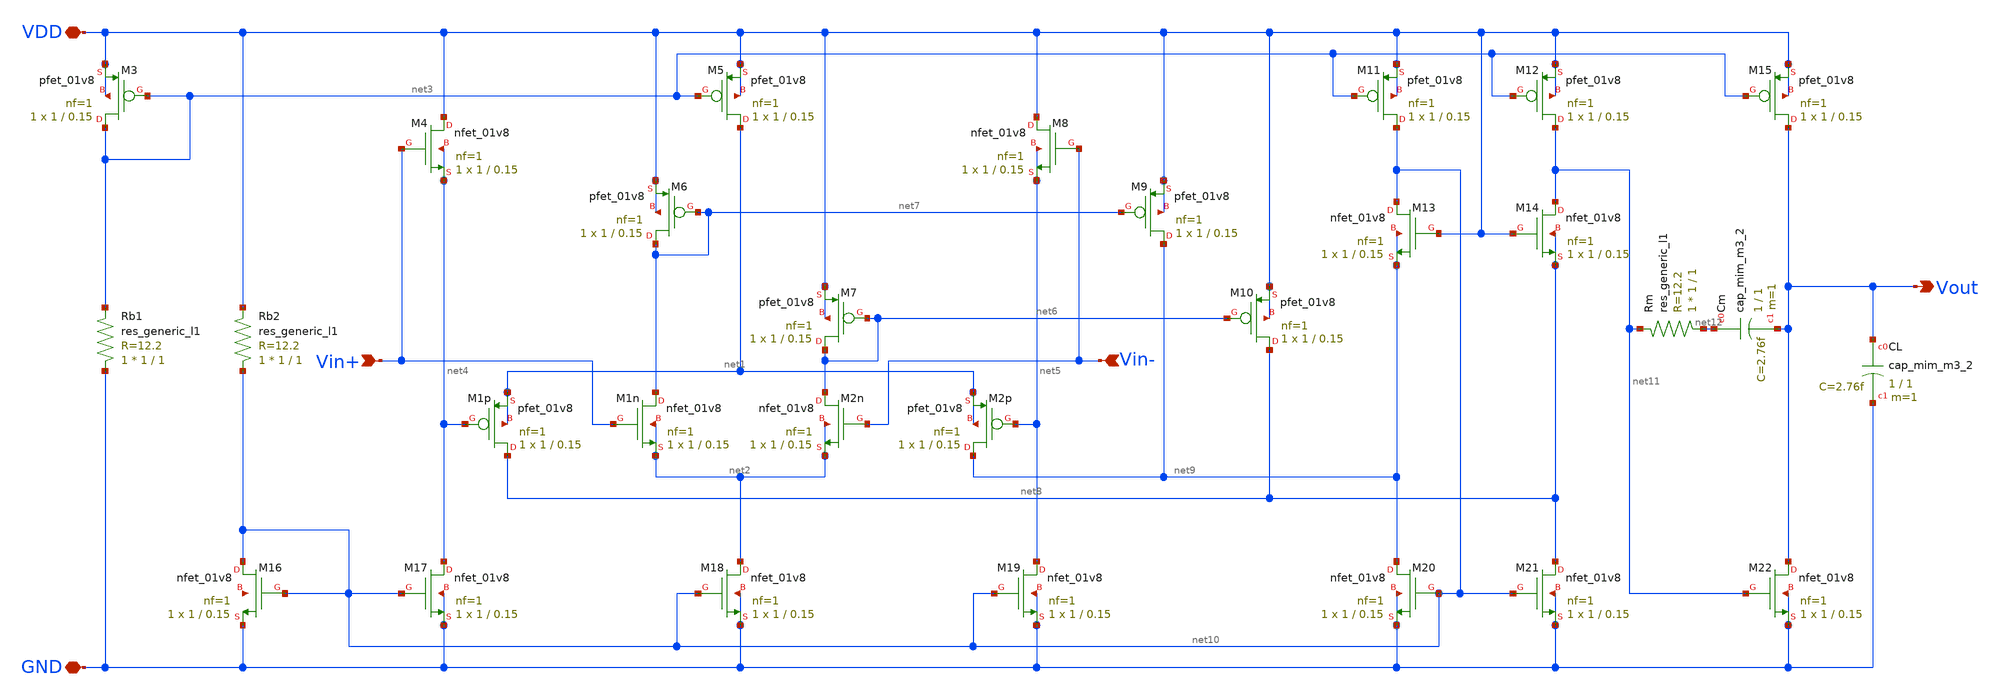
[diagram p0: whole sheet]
** sch_path: charge-pump/charge-pump-amplifier.sch
**.subckt charge-pump-amplifier Vin+ Vin- Vout VDD GND
*.ipin Vin+
*.ipin Vin-
*.opin Vout
*.iopin VDD
*.iopin GND
XM1p net8 net4 net1 net1 sky130_fd_pr__pfet_01v8 L=0.15 W=1 nf=1 ad='int((nf+1)/2) * W/nf * 0.29' as='int((nf+2)/2) * W/nf * 0.29'
+ pd='2*int((nf+1)/2) * (W/nf + 0.29)' ps='2*int((nf+2)/2) * (W/nf + 0.29)' nrd='0.29 / W' nrs='0.29 / W'
+ sa=0 sb=0 sd=0 mult=1 m=1
XM1n net7 Vin+ net2 net2 sky130_fd_pr__nfet_01v8 L=0.15 W=1 nf=1 ad='int((nf+1)/2) * W/nf * 0.29' as='int((nf+2)/2) * W/nf * 0.29'
+ pd='2*int((nf+1)/2) * (W/nf + 0.29)' ps='2*int((nf+2)/2) * (W/nf + 0.29)' nrd='0.29 / W' nrs='0.29 / W'
+ sa=0 sb=0 sd=0 mult=1 m=1
XM2n net6 Vin- net2 net2 sky130_fd_pr__nfet_01v8 L=0.15 W=1 nf=1 ad='int((nf+1)/2) * W/nf * 0.29' as='int((nf+2)/2) * W/nf * 0.29'
+ pd='2*int((nf+1)/2) * (W/nf + 0.29)' ps='2*int((nf+2)/2) * (W/nf + 0.29)' nrd='0.29 / W' nrs='0.29 / W'
+ sa=0 sb=0 sd=0 mult=1 m=1
XM2p net9 net5 net1 net1 sky130_fd_pr__pfet_01v8 L=0.15 W=1 nf=1 ad='int((nf+1)/2) * W/nf * 0.29' as='int((nf+2)/2) * W/nf * 0.29'
+ pd='2*int((nf+1)/2) * (W/nf + 0.29)' ps='2*int((nf+2)/2) * (W/nf + 0.29)' nrd='0.29 / W' nrs='0.29 / W'
+ sa=0 sb=0 sd=0 mult=1 m=1
XM3 net3 net3 VDD VDD sky130_fd_pr__pfet_01v8 L=0.15 W=1 nf=1 ad='int((nf+1)/2) * W/nf * 0.29' as='int((nf+2)/2) * W/nf * 0.29'
+ pd='2*int((nf+1)/2) * (W/nf + 0.29)' ps='2*int((nf+2)/2) * (W/nf + 0.29)' nrd='0.29 / W' nrs='0.29 / W'
+ sa=0 sb=0 sd=0 mult=1 m=1
XM4 VDD Vin+ net4 net4 sky130_fd_pr__nfet_01v8 L=0.15 W=1 nf=1 ad='int((nf+1)/2) * W/nf * 0.29' as='int((nf+2)/2) * W/nf * 0.29'
+ pd='2*int((nf+1)/2) * (W/nf + 0.29)' ps='2*int((nf+2)/2) * (W/nf + 0.29)' nrd='0.29 / W' nrs='0.29 / W'
+ sa=0 sb=0 sd=0 mult=1 m=1
XM5 net1 net3 VDD VDD sky130_fd_pr__pfet_01v8 L=0.15 W=1 nf=1 ad='int((nf+1)/2) * W/nf * 0.29' as='int((nf+2)/2) * W/nf * 0.29'
+ pd='2*int((nf+1)/2) * (W/nf + 0.29)' ps='2*int((nf+2)/2) * (W/nf + 0.29)' nrd='0.29 / W' nrs='0.29 / W'
+ sa=0 sb=0 sd=0 mult=1 m=1
XM6 net7 net7 VDD VDD sky130_fd_pr__pfet_01v8 L=0.15 W=1 nf=1 ad='int((nf+1)/2) * W/nf * 0.29' as='int((nf+2)/2) * W/nf * 0.29'
+ pd='2*int((nf+1)/2) * (W/nf + 0.29)' ps='2*int((nf+2)/2) * (W/nf + 0.29)' nrd='0.29 / W' nrs='0.29 / W'
+ sa=0 sb=0 sd=0 mult=1 m=1
XM7 net6 net6 VDD VDD sky130_fd_pr__pfet_01v8 L=0.15 W=1 nf=1 ad='int((nf+1)/2) * W/nf * 0.29' as='int((nf+2)/2) * W/nf * 0.29'
+ pd='2*int((nf+1)/2) * (W/nf + 0.29)' ps='2*int((nf+2)/2) * (W/nf + 0.29)' nrd='0.29 / W' nrs='0.29 / W'
+ sa=0 sb=0 sd=0 mult=1 m=1
XM8 VDD Vin- net5 net5 sky130_fd_pr__nfet_01v8 L=0.15 W=1 nf=1 ad='int((nf+1)/2) * W/nf * 0.29' as='int((nf+2)/2) * W/nf * 0.29'
+ pd='2*int((nf+1)/2) * (W/nf + 0.29)' ps='2*int((nf+2)/2) * (W/nf + 0.29)' nrd='0.29 / W' nrs='0.29 / W'
+ sa=0 sb=0 sd=0 mult=1 m=1
XM9 net9 net7 VDD VDD sky130_fd_pr__pfet_01v8 L=0.15 W=1 nf=1 ad='int((nf+1)/2) * W/nf * 0.29' as='int((nf+2)/2) * W/nf * 0.29'
+ pd='2*int((nf+1)/2) * (W/nf + 0.29)' ps='2*int((nf+2)/2) * (W/nf + 0.29)' nrd='0.29 / W' nrs='0.29 / W'
+ sa=0 sb=0 sd=0 mult=1 m=1
XM10 net8 net6 VDD VDD sky130_fd_pr__pfet_01v8 L=0.15 W=1 nf=1 ad='int((nf+1)/2) * W/nf * 0.29' as='int((nf+2)/2) * W/nf * 0.29'
+ pd='2*int((nf+1)/2) * (W/nf + 0.29)' ps='2*int((nf+2)/2) * (W/nf + 0.29)' nrd='0.29 / W' nrs='0.29 / W'
+ sa=0 sb=0 sd=0 mult=1 m=1
XM11 net10 net3 VDD VDD sky130_fd_pr__pfet_01v8 L=0.15 W=1 nf=1 ad='int((nf+1)/2) * W/nf * 0.29' as='int((nf+2)/2) * W/nf * 0.29'
+ pd='2*int((nf+1)/2) * (W/nf + 0.29)' ps='2*int((nf+2)/2) * (W/nf + 0.29)' nrd='0.29 / W' nrs='0.29 / W'
+ sa=0 sb=0 sd=0 mult=1 m=1
XM12 net11 net3 VDD VDD sky130_fd_pr__pfet_01v8 L=0.15 W=1 nf=1 ad='int((nf+1)/2) * W/nf * 0.29' as='int((nf+2)/2) * W/nf * 0.29'
+ pd='2*int((nf+1)/2) * (W/nf + 0.29)' ps='2*int((nf+2)/2) * (W/nf + 0.29)' nrd='0.29 / W' nrs='0.29 / W'
+ sa=0 sb=0 sd=0 mult=1 m=1
XM13 net10 VDD net9 net9 sky130_fd_pr__nfet_01v8 L=0.15 W=1 nf=1 ad='int((nf+1)/2) * W/nf * 0.29' as='int((nf+2)/2) * W/nf * 0.29'
+ pd='2*int((nf+1)/2) * (W/nf + 0.29)' ps='2*int((nf+2)/2) * (W/nf + 0.29)' nrd='0.29 / W' nrs='0.29 / W'
+ sa=0 sb=0 sd=0 mult=1 m=1
XM14 net11 VDD net8 net8 sky130_fd_pr__nfet_01v8 L=0.15 W=1 nf=1 ad='int((nf+1)/2) * W/nf * 0.29' as='int((nf+2)/2) * W/nf * 0.29'
+ pd='2*int((nf+1)/2) * (W/nf + 0.29)' ps='2*int((nf+2)/2) * (W/nf + 0.29)' nrd='0.29 / W' nrs='0.29 / W'
+ sa=0 sb=0 sd=0 mult=1 m=1
XM15 Vout net3 VDD VDD sky130_fd_pr__pfet_01v8 L=0.15 W=1 nf=1 ad='int((nf+1)/2) * W/nf * 0.29' as='int((nf+2)/2) * W/nf * 0.29'
+ pd='2*int((nf+1)/2) * (W/nf + 0.29)' ps='2*int((nf+2)/2) * (W/nf + 0.29)' nrd='0.29 / W' nrs='0.29 / W'
+ sa=0 sb=0 sd=0 mult=1 m=1
XM16 net10 net10 GND net13 sky130_fd_pr__nfet_01v8 L=0.15 W=1 nf=1 ad='int((nf+1)/2) * W/nf * 0.29' as='int((nf+2)/2) * W/nf * 0.29'
+ pd='2*int((nf+1)/2) * (W/nf + 0.29)' ps='2*int((nf+2)/2) * (W/nf + 0.29)' nrd='0.29 / W' nrs='0.29 / W'
+ sa=0 sb=0 sd=0 mult=1 m=1
XM17 net4 net10 GND GND sky130_fd_pr__nfet_01v8 L=0.15 W=1 nf=1 ad='int((nf+1)/2) * W/nf * 0.29' as='int((nf+2)/2) * W/nf * 0.29'
+ pd='2*int((nf+1)/2) * (W/nf + 0.29)' ps='2*int((nf+2)/2) * (W/nf + 0.29)' nrd='0.29 / W' nrs='0.29 / W'
+ sa=0 sb=0 sd=0 mult=1 m=1
XM18 net2 net10 GND GND sky130_fd_pr__nfet_01v8 L=0.15 W=1 nf=1 ad='int((nf+1)/2) * W/nf * 0.29' as='int((nf+2)/2) * W/nf * 0.29'
+ pd='2*int((nf+1)/2) * (W/nf + 0.29)' ps='2*int((nf+2)/2) * (W/nf + 0.29)' nrd='0.29 / W' nrs='0.29 / W'
+ sa=0 sb=0 sd=0 mult=1 m=1
XM19 net5 net10 GND GND sky130_fd_pr__nfet_01v8 L=0.15 W=1 nf=1 ad='int((nf+1)/2) * W/nf * 0.29' as='int((nf+2)/2) * W/nf * 0.29'
+ pd='2*int((nf+1)/2) * (W/nf + 0.29)' ps='2*int((nf+2)/2) * (W/nf + 0.29)' nrd='0.29 / W' nrs='0.29 / W'
+ sa=0 sb=0 sd=0 mult=1 m=1
XM20 net9 net10 GND GND sky130_fd_pr__nfet_01v8 L=0.15 W=1 nf=1 ad='int((nf+1)/2) * W/nf * 0.29' as='int((nf+2)/2) * W/nf * 0.29'
+ pd='2*int((nf+1)/2) * (W/nf + 0.29)' ps='2*int((nf+2)/2) * (W/nf + 0.29)' nrd='0.29 / W' nrs='0.29 / W'
+ sa=0 sb=0 sd=0 mult=1 m=1
XM21 net8 net10 GND GND sky130_fd_pr__nfet_01v8 L=0.15 W=1 nf=1 ad='int((nf+1)/2) * W/nf * 0.29' as='int((nf+2)/2) * W/nf * 0.29'
+ pd='2*int((nf+1)/2) * (W/nf + 0.29)' ps='2*int((nf+2)/2) * (W/nf + 0.29)' nrd='0.29 / W' nrs='0.29 / W'
+ sa=0 sb=0 sd=0 mult=1 m=1
XM22 Vout net11 GND GND sky130_fd_pr__nfet_01v8 L=0.15 W=1 nf=1 ad='int((nf+1)/2) * W/nf * 0.29' as='int((nf+2)/2) * W/nf * 0.29'
+ pd='2*int((nf+1)/2) * (W/nf + 0.29)' ps='2*int((nf+2)/2) * (W/nf + 0.29)' nrd='0.29 / W' nrs='0.29 / W'
+ sa=0 sb=0 sd=0 mult=1 m=1
Rb1 GND net3 sky130_fd_pr__res_generic_l1 W=1 L=1 m=1
Rb2 net10 VDD sky130_fd_pr__res_generic_l1 W=1 L=1 m=1
Rm net12 net11 sky130_fd_pr__res_generic_l1 W=1 L=1 m=1
XCm net12 Vout sky130_fd_pr__cap_mim_m3_2 W=1 L=1 MF=1 m=1
XCL Vout GND sky130_fd_pr__cap_mim_m3_2 W=1 L=1 MF=1 m=1
**.ends
.end
